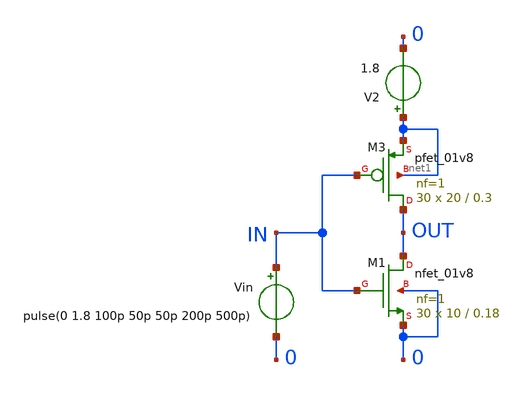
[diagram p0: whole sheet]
** sch_path: inverter.sch
**.subckt inverter
XM1 OUT IN 0 0 sky130_fd_pr__nfet_01v8 L=0.18 W=10 nf=1 ad='W * 0.29' as='W * 0.29' pd='2 * (W + 0.29)'
+ ps='2 * (W + 0.29)' nrd='0.29 / W' nrs='0.29 / W' sa=0 sb=0 sd=0 mult=30 m=30
V2 net1 0 1.8
Vin IN 0 pulse(0 1.8 100p 50p 50p 200p 500p)
XM3 OUT IN net1 net1 sky130_fd_pr__pfet_01v8 L=0.3 W=20 nf=1 ad='int((nf+1)/2) * W/nf * 0.29' as='int((nf+2)/2) * W/nf * 0.29'
+ pd='2*int((nf+1)/2) * (W/nf + 0.29)' ps='2*int((nf+2)/2) * (W/nf + 0.29)' nrd='0.29 / W' nrs='0.29 / W'
+ sa=0 sb=0 sd=0 mult=30 m=30
**** begin user architecture code



* Include Models
.lib ~/skywater/skywater-pdk/libraries/sky130_fd_pr/latest/models/sky130.lib.spice tt
.tran 3p 600ps
.save all


**** end user architecture code
**.ends
.end
